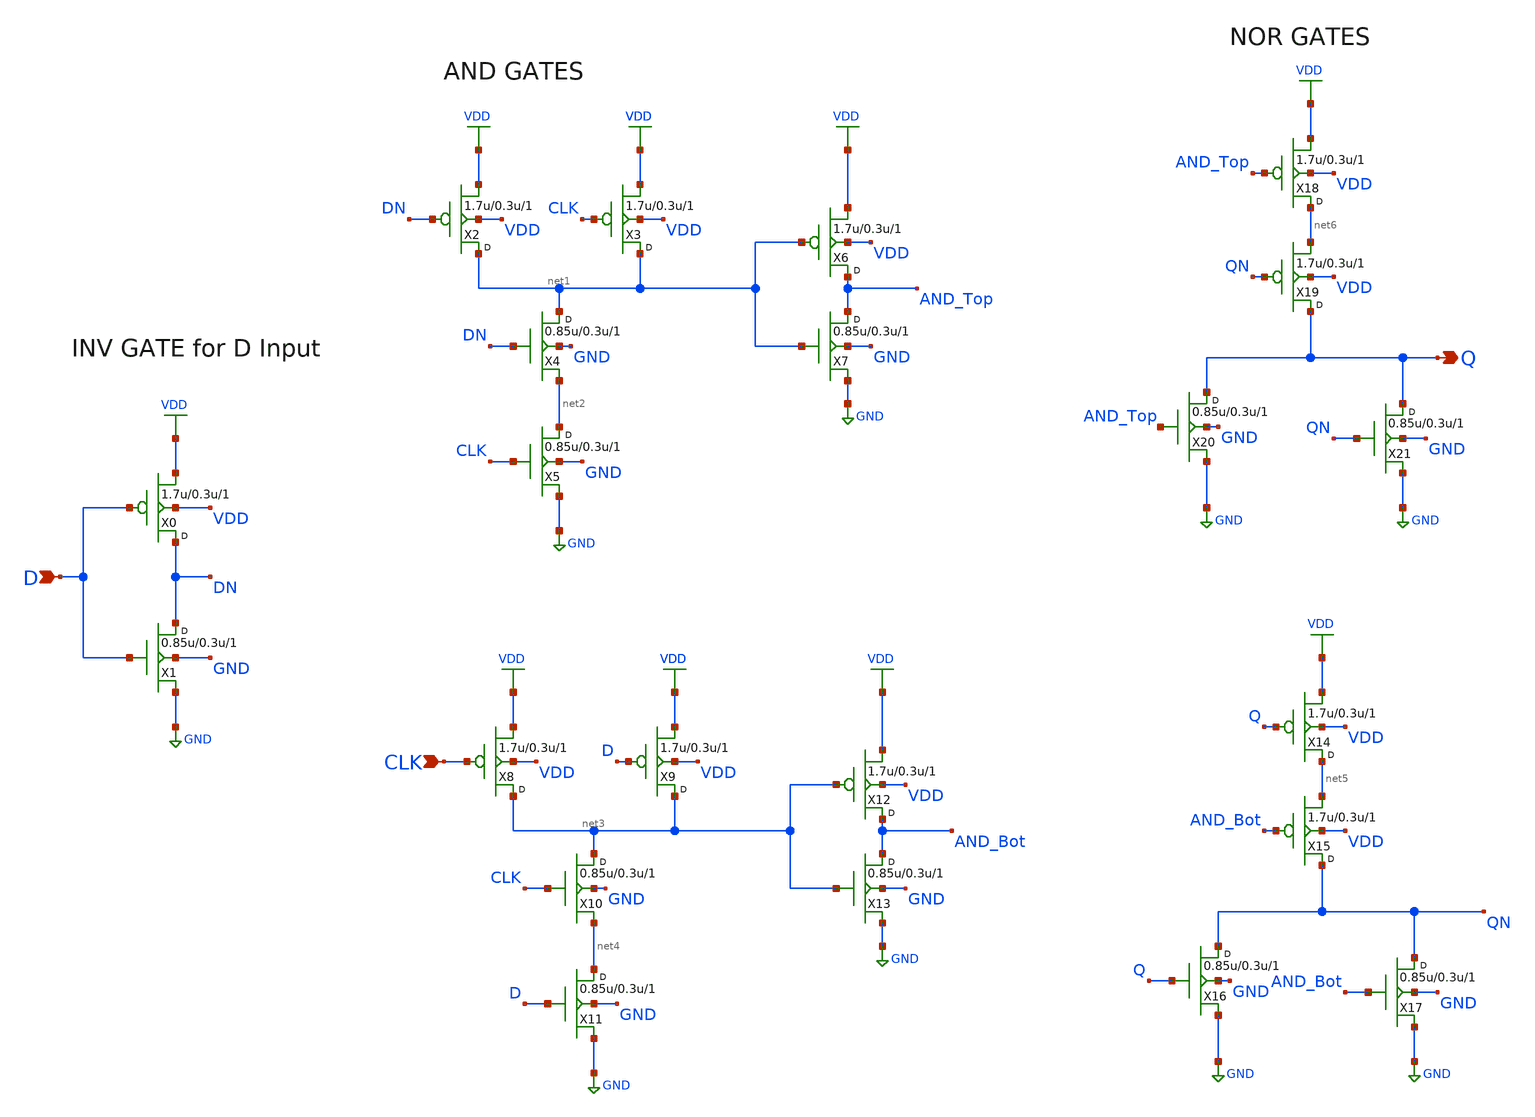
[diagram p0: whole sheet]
** sch_path: openfasoc/common/platforms/gf180osu9t/lib/dlat1/gf180mcu_osu_sc_dlat_1.sch
**.subckt gf180mcu_osu_sc_dlat_1 D CLK Q
*.ipin D
*.ipin CLK
*.opin Q
X0 DN D VDD VDD pmos_3p3 w=1.7u l=0.3u m=1
X1 DN D GND GND nmos_3p3 w=0.85u l=0.3u m=1
X2 net1 DN VDD VDD pmos_3p3 w=1.7u l=0.3u m=1
X3 net1 CLK VDD VDD pmos_3p3 w=1.7u l=0.3u m=1
X4 net1 DN net2 GND nmos_3p3 w=0.85u l=0.3u m=1
X5 net2 CLK GND GND nmos_3p3 w=0.85u l=0.3u m=1
X6 AND_Top net1 VDD VDD pmos_3p3 w=1.7u l=0.3u m=1
X7 AND_Top net1 GND GND nmos_3p3 w=0.85u l=0.3u m=1
X8 net3 CLK VDD VDD pmos_3p3 w=1.7u l=0.3u m=1
X9 net3 D VDD VDD pmos_3p3 w=1.7u l=0.3u m=1
X10 net3 CLK net4 GND nmos_3p3 w=0.85u l=0.3u m=1
X11 net4 D GND GND nmos_3p3 w=0.85u l=0.3u m=1
X12 AND_Bot net3 VDD VDD pmos_3p3 w=1.7u l=0.3u m=1
X13 AND_Bot net3 GND GND nmos_3p3 w=0.85u l=0.3u m=1
X14 net5 Q VDD VDD pmos_3p3 w=1.7u l=0.3u m=1
X15 QN AND_Bot net5 VDD pmos_3p3 w=1.7u l=0.3u m=1
X16 QN Q GND GND nmos_3p3 w=0.85u l=0.3u m=1
X17 QN AND_Bot GND GND nmos_3p3 w=0.85u l=0.3u m=1
X18 net6 AND_Top VDD VDD pmos_3p3 w=1.7u l=0.3u m=1
X19 Q QN net6 VDD pmos_3p3 w=1.7u l=0.3u m=1
X20 Q AND_Top GND GND nmos_3p3 w=0.85u l=0.3u m=1
X21 Q QN GND GND nmos_3p3 w=0.85u l=0.3u m=1
**.ends
.GLOBAL VDD
.GLOBAL GND
.end
